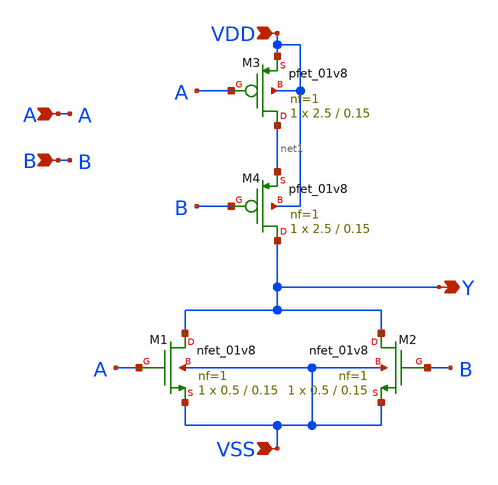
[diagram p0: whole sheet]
** sch_path: nor_FFD.sch
**.subckt nor_FFD VDD A B VSS Y
*.ipin VDD
*.ipin A
*.ipin B
*.ipin VSS
*.opin Y
XM1 Y A VSS VSS sky130_fd_pr__nfet_01v8 L=0.15 W=0.5 nf=1 ad='int((nf+1)/2) * W/nf * 0.29' as='int((nf+2)/2) * W/nf * 0.29'
+ pd='2*int((nf+1)/2) * (W/nf + 0.29)' ps='2*int((nf+2)/2) * (W/nf + 0.29)' nrd='0.29 / W' nrs='0.29 / W'
+ sa=0 sb=0 sd=0 mult=1 m=1
XM2 Y B VSS VSS sky130_fd_pr__nfet_01v8 L=0.15 W=0.5 nf=1 ad='int((nf+1)/2) * W/nf * 0.29' as='int((nf+2)/2) * W/nf * 0.29'
+ pd='2*int((nf+1)/2) * (W/nf + 0.29)' ps='2*int((nf+2)/2) * (W/nf + 0.29)' nrd='0.29 / W' nrs='0.29 / W'
+ sa=0 sb=0 sd=0 mult=1 m=1
XM3 net1 A VDD VDD sky130_fd_pr__pfet_01v8 L=0.15 W=2.5 nf=1 ad='int((nf+1)/2) * W/nf * 0.29' as='int((nf+2)/2) * W/nf * 0.29'
+ pd='2*int((nf+1)/2) * (W/nf + 0.29)' ps='2*int((nf+2)/2) * (W/nf + 0.29)' nrd='0.29 / W' nrs='0.29 / W'
+ sa=0 sb=0 sd=0 mult=1 m=1
XM4 Y B net1 VDD sky130_fd_pr__pfet_01v8 L=0.15 W=2.5 nf=1 ad='int((nf+1)/2) * W/nf * 0.29' as='int((nf+2)/2) * W/nf * 0.29'
+ pd='2*int((nf+1)/2) * (W/nf + 0.29)' ps='2*int((nf+2)/2) * (W/nf + 0.29)' nrd='0.29 / W' nrs='0.29 / W'
+ sa=0 sb=0 sd=0 mult=1 m=1
**.ends
.end
